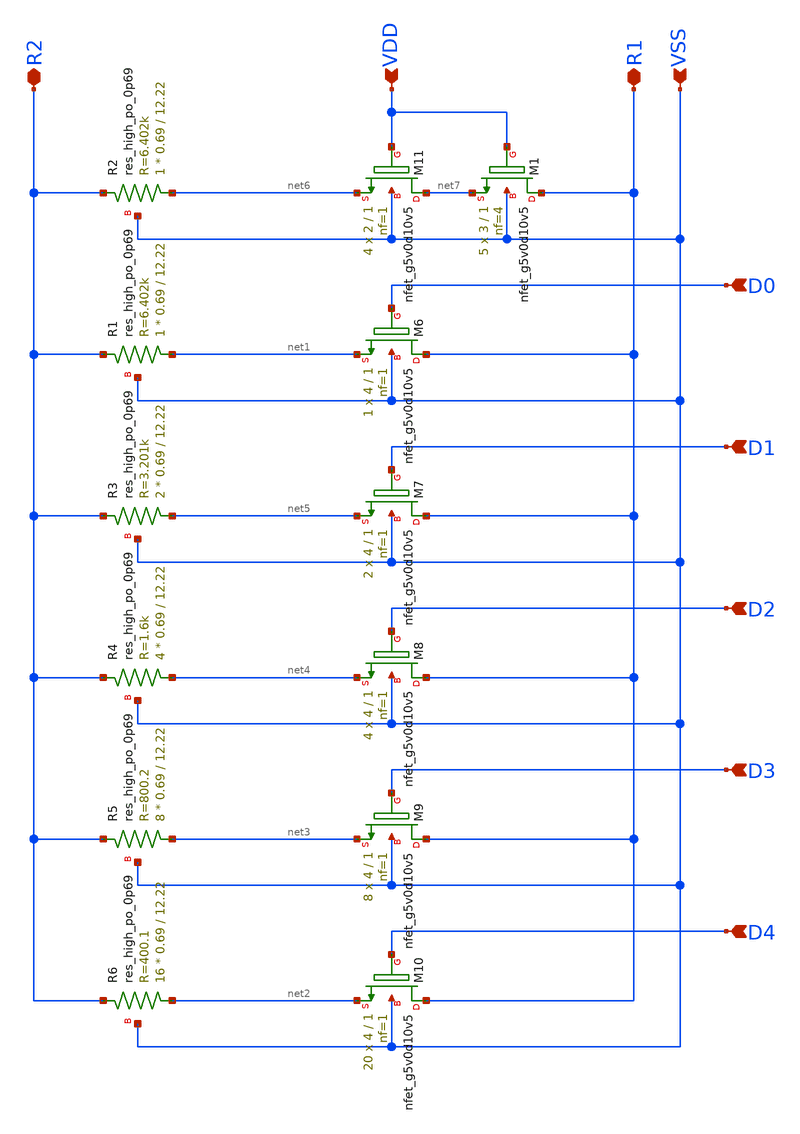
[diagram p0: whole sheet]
** sch_path: xschem/RB_array_10.sch
**.subckt RB_array_10 VSS R2 D0 D1 D2 D3 D4 R1 VDD
*.ipin VSS
*.iopin R2
*.ipin D0
*.ipin D1
*.ipin D2
*.ipin D3
*.ipin D4
*.iopin R1
*.ipin VDD
XR2 net6 R2 VSS sky130_fd_pr__res_high_po_0p69 L=12.22 mult=1 m=1
XR1 net1 R2 VSS sky130_fd_pr__res_high_po_0p69 L=12.22 mult=1 m=1
XR3 net5 R2 VSS sky130_fd_pr__res_high_po_0p69 L=12.22 mult=2 m=2
XR4 net4 R2 VSS sky130_fd_pr__res_high_po_0p69 L=12.22 mult=4 m=4
XR5 net3 R2 VSS sky130_fd_pr__res_high_po_0p69 L=12.22 mult=8 m=8
XR6 net2 R2 VSS sky130_fd_pr__res_high_po_0p69 L=12.22 mult=16 m=16
XM6 R1 D0 net1 VSS sky130_fd_pr__nfet_g5v0d10v5 L=1 W=4 nf=1 ad='int((nf+1)/2) * W/nf * 0.29' as='int((nf+2)/2) * W/nf * 0.29'
+ pd='2*int((nf+1)/2) * (W/nf + 0.29)' ps='2*int((nf+2)/2) * (W/nf + 0.29)' nrd='0.29 / W' nrs='0.29 / W'
+ sa=0 sb=0 sd=0 mult=1 m=1
XM7 R1 D1 net5 VSS sky130_fd_pr__nfet_g5v0d10v5 L=1 W=4 nf=1 ad='int((nf+1)/2) * W/nf * 0.29' as='int((nf+2)/2) * W/nf * 0.29'
+ pd='2*int((nf+1)/2) * (W/nf + 0.29)' ps='2*int((nf+2)/2) * (W/nf + 0.29)' nrd='0.29 / W' nrs='0.29 / W'
+ sa=0 sb=0 sd=0 mult=2 m=2
XM8 R1 D2 net4 VSS sky130_fd_pr__nfet_g5v0d10v5 L=1 W=4 nf=1 ad='int((nf+1)/2) * W/nf * 0.29' as='int((nf+2)/2) * W/nf * 0.29'
+ pd='2*int((nf+1)/2) * (W/nf + 0.29)' ps='2*int((nf+2)/2) * (W/nf + 0.29)' nrd='0.29 / W' nrs='0.29 / W'
+ sa=0 sb=0 sd=0 mult=4 m=4
XM9 R1 D3 net3 VSS sky130_fd_pr__nfet_g5v0d10v5 L=1 W=4 nf=1 ad='int((nf+1)/2) * W/nf * 0.29' as='int((nf+2)/2) * W/nf * 0.29'
+ pd='2*int((nf+1)/2) * (W/nf + 0.29)' ps='2*int((nf+2)/2) * (W/nf + 0.29)' nrd='0.29 / W' nrs='0.29 / W'
+ sa=0 sb=0 sd=0 mult=8 m=8
XM10 R1 D4 net2 VSS sky130_fd_pr__nfet_g5v0d10v5 L=1 W=4 nf=1 ad='int((nf+1)/2) * W/nf * 0.29' as='int((nf+2)/2) * W/nf * 0.29'
+ pd='2*int((nf+1)/2) * (W/nf + 0.29)' ps='2*int((nf+2)/2) * (W/nf + 0.29)' nrd='0.29 / W' nrs='0.29 / W'
+ sa=0 sb=0 sd=0 mult=20 m=20
XM11 net7 VDD net6 VSS sky130_fd_pr__nfet_g5v0d10v5 L=1 W=2 nf=1 ad='int((nf+1)/2) * W/nf * 0.29' as='int((nf+2)/2) * W/nf * 0.29'
+ pd='2*int((nf+1)/2) * (W/nf + 0.29)' ps='2*int((nf+2)/2) * (W/nf + 0.29)' nrd='0.29 / W' nrs='0.29 / W'
+ sa=0 sb=0 sd=0 mult=4 m=4
XM1 R1 VDD net7 VSS sky130_fd_pr__nfet_g5v0d10v5 L=1 W=3 nf=4 ad='int((nf+1)/2) * W/nf * 0.29' as='int((nf+2)/2) * W/nf * 0.29'
+ pd='2*int((nf+1)/2) * (W/nf + 0.29)' ps='2*int((nf+2)/2) * (W/nf + 0.29)' nrd='0.29 / W' nrs='0.29 / W'
+ sa=0 sb=0 sd=0 mult=5 m=5
**.ends
.end
